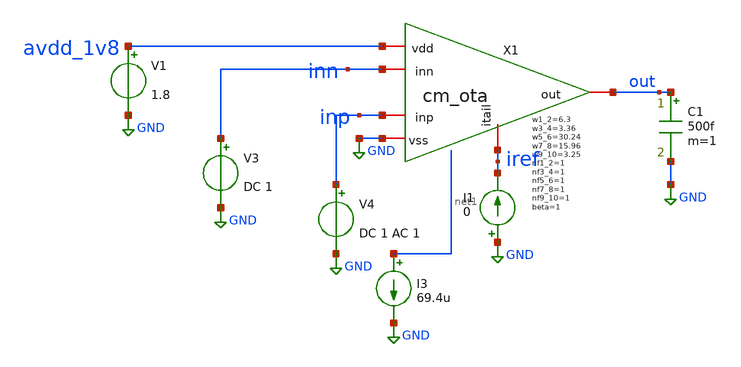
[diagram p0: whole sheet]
** sch_path: ISSCC25/submitted_notebooks/current_mirror_ota_optimization/characterization/sky130/schematics/tb_cm_ota_working_v2_extracted_ac_to_layout.sch
**.subckt tb_cm_ota_working_v2_extracted_ac_to_layout
V1 avdd_1v8 GND 1.8
C1 out GND 500f m=1
V3 inn GND DC 1
V4 inp GND DC 1 AC 1
X1 avdd_1v8 out inp inn iref GND cm_ota w1_2=6.3 w3_4=3.36 w5_6=30.24 w7_8=15.96 w9_10=3.25 beta=1
+ nf1_2=1 nf3_4=1 nf5_6=1 nf7_8=1 nf9_10=1
I1 GND iref 0
I3 net1 GND 69.4u
**** begin user architecture code

** opencircuitdesign pdks isntsall
.lib /opt/pdk/open_pdks/sky130/sky130A/libs.tech/ngspice/sky130.lib.spice tt





.temp 27
.option savecurrents
.save all
.control
	ac dec 100 1 1e15
	plot vdb(out) vs frequency
	plot (180*cph(out)/pi) vs frequency
	let phase_vector = 180*cph(out)/pi
	let gain_vector = vdb(out)
	meas ac unity_gain_freq_val when vdb(out)=0
	meas ac dc_gain_val find vdb(out) at=10Hz
	let dc_gain = dc_gain_val
	meas ac p1_val when phase_vector=-45 cross=1
	meas ac p2_val when phase_vector=-135 cross=1
	meas ac three_db when gain_vector=dc_gain_val -3 cross=1
	let p2 = p2_val
	let p1 = p1_val
	let dc_gain = dc_gain_val
	let unity_gain_freq = unity_gain_freq_val
	op
	write tb_cm_ota_working_v2_extracted_ac.raw
	let gm1 = @m.x1.xm1.msky130_fd_pr__nfet_01v8[gm]
	let gm2 = @m.x1.xm2.msky130_fd_pr__nfet_01v8[gm]
	let gm3 = @m.x1.xm3.msky130_fd_pr__pfet_01v8[gm]
	let gm4 = @m.x1.xm4.msky130_fd_pr__pfet_01v8[gm]
	let gm5 = @m.x1.xm5.msky130_fd_pr__nfet_01v8[gm]
	let gm6 = @m.x1.xm6.msky130_fd_pr__nfet_01v8[gm]
	let gm7 = @m.x1.xm7.msky130_fd_pr__pfet_01v8[gm]
	let gm8 = @m.x1.xm8.msky130_fd_pr__pfet_01v8[gm]

	let id1 = @m.x1.xm1.msky130_fd_pr__nfet_01v8[id]
	let id2 = @m.x1.xm2.msky130_fd_pr__nfet_01v8[id]
	let id3 = @m.x1.xm3.msky130_fd_pr__pfet_01v8[id]
	let id4 = @m.x1.xm4.msky130_fd_pr__pfet_01v8[id]
	let id5 = @m.x1.xm5.msky130_fd_pr__nfet_01v8[id]
	let id6 = @m.x1.xm6.msky130_fd_pr__nfet_01v8[id]
	let id7 = @m.x1.xm7.msky130_fd_pr__pfet_01v8[id]
	let id8 = @m.x1.xm8.msky130_fd_pr__pfet_01v8[id]

	let current_scale = id5/id1

	let kgm1 = gm1/id1
	let kgm2 = gm2/id2
	let kgm3 = gm3/id3
	let kgm4 = gm4/id4
	let kgm5 = gm5/id5
	let kgm6 = gm6/id6
	let kgm7 = gm7/id7
	let kgm8 = gm8/id8

	print kgm1
	print kgm2
	print kgm3
	print kgm4
	print kgm5
	print kgm6
	print kgm7
	print kgm8

	print id1
	print id2
	print id3
	print id4
	print id5
	print id6
	print id7
	print id8

	print current_scale
	print dc_gain_val
	print p1_val
	print p2_val
.endc


**** end user architecture code
**.ends

* expanding   symbol:  cm_ota.sym # of pins=6
** sym_path: ISSCC25/submitted_notebooks/current_mirror_ota_optimization/characterization/sky130/schematics/cm_ota.sym
** sch_path: ISSCC25/submitted_notebooks/current_mirror_ota_optimization/characterization/sky130/schematics/cm_ota.sch
.subckt cm_ota vdd out inp inn itail vss  w1_2=1 w3_4=1 w5_6=1 w7_8=1 w9_10=1 beta=2 nf1_2=2 nf3_4=2
+ nf5_6=2 nf7_8=2 nf9_10=2
*.iopin inn
*.iopin inp
*.iopin out
*.iopin vss
*.iopin vdd
*.iopin itail
XM1 ds1_3 inn source source sky130_fd_pr__nfet_01v8 L=0.15 W=w1_2 nf=nf1_2 ad='int((nf+1)/2) * W/nf * 0.29'
+ as='int((nf+2)/2) * W/nf * 0.29' pd='2*int((nf+1)/2) * (W/nf + 0.29)' ps='2*int((nf+2)/2) * (W/nf + 0.29)'
+ nrd='0.29 / W' nrs='0.29 / W' sa=0 sb=0 sd=0 mult=1 m=1
xM3 ds1_3 ds1_3 vdd vdd sky130_fd_pr__pfet_01v8 L=0.15 W=w3_4 nf=nf3_4 ad='int((nf+1)/2) * W/nf * 0.29'
+ as='int((nf+2)/2) * W/nf * 0.29' pd='2*int((nf+1)/2) * (W/nf + 0.29)' ps='2*int((nf+2)/2) * (W/nf + 0.29)'
+ nrd='0.29 / W' nrs='0.29 / W' sa=0 sb=0 sd=0 mult=1 m=1
XM2 ds2_4 inp source source sky130_fd_pr__nfet_01v8 L=0.15 W=w1_2 nf=nf1_2 ad='int((nf+1)/2) * W/nf * 0.29'
+ as='int((nf+2)/2) * W/nf * 0.29' pd='2*int((nf+1)/2) * (W/nf + 0.29)' ps='2*int((nf+2)/2) * (W/nf + 0.29)'
+ nrd='0.29 / W' nrs='0.29 / W' sa=0 sb=0 sd=0 mult=1 m=1
xM4 ds2_4 ds2_4 vdd vdd sky130_fd_pr__pfet_01v8 L=0.15 W=w3_4 nf=nf3_4 ad='int((nf+1)/2) * W/nf * 0.29'
+ as='int((nf+2)/2) * W/nf * 0.29' pd='2*int((nf+1)/2) * (W/nf + 0.29)' ps='2*int((nf+2)/2) * (W/nf + 0.29)'
+ nrd='0.29 / W' nrs='0.29 / W' sa=0 sb=0 sd=0 mult=1 m=1
xM7 ds5_7 ds1_3 vdd vdd sky130_fd_pr__pfet_01v8 L=0.15 W=w7_8 nf=nf7_8 ad='int((nf+1)/2) * W/nf * 0.29'
+ as='int((nf+2)/2) * W/nf * 0.29' pd='2*int((nf+1)/2) * (W/nf + 0.29)' ps='2*int((nf+2)/2) * (W/nf + 0.29)'
+ nrd='0.29 / W' nrs='0.29 / W' sa=0 sb=0 sd=0 mult=1 m=1
XM5 ds5_7 ds5_7 vss vss sky130_fd_pr__nfet_01v8 L=0.15 W=w5_6 nf=nf5_6 ad='int((nf+1)/2) * W/nf * 0.29'
+ as='int((nf+2)/2) * W/nf * 0.29' pd='2*int((nf+1)/2) * (W/nf + 0.29)' ps='2*int((nf+2)/2) * (W/nf + 0.29)'
+ nrd='0.29 / W' nrs='0.29 / W' sa=0 sb=0 sd=0 mult=1 m=1
XM6 out ds5_7 vss vss sky130_fd_pr__nfet_01v8 L=0.15 W=w5_6 nf=nf5_6 ad='int((nf+1)/2) * W/nf * 0.29'
+ as='int((nf+2)/2) * W/nf * 0.29' pd='2*int((nf+1)/2) * (W/nf + 0.29)' ps='2*int((nf+2)/2) * (W/nf + 0.29)'
+ nrd='0.29 / W' nrs='0.29 / W' sa=0 sb=0 sd=0 mult=1 m=1
xM8 out ds2_4 vdd vdd sky130_fd_pr__pfet_01v8 L=0.15 W=w7_8 nf=nf7_8 ad='int((nf+1)/2) * W/nf * 0.29'
+ as='int((nf+2)/2) * W/nf * 0.29' pd='2*int((nf+1)/2) * (W/nf + 0.29)' ps='2*int((nf+2)/2) * (W/nf + 0.29)'
+ nrd='0.29 / W' nrs='0.29 / W' sa=0 sb=0 sd=0 mult=1 m=1
XM9 source itail vss vss sky130_fd_pr__nfet_01v8 L=0.15 W=w9_10 nf=nf9_10 ad='int((nf+1)/2) * W/nf * 0.29'
+ as='int((nf+2)/2) * W/nf * 0.29' pd='2*int((nf+1)/2) * (W/nf + 0.29)' ps='2*int((nf+2)/2) * (W/nf + 0.29)'
+ nrd='0.29 / W' nrs='0.29 / W' sa=0 sb=0 sd=0 mult=1 m=1
XM10 itail itail vss vss sky130_fd_pr__nfet_01v8 L=0.15 W=w9_10 nf=nf1_2 ad='int((nf+1)/2) * W/nf * 0.29'
+ as='int((nf+2)/2) * W/nf * 0.29' pd='2*int((nf+1)/2) * (W/nf + 0.29)' ps='2*int((nf+2)/2) * (W/nf + 0.29)'
+ nrd='0.29 / W' nrs='0.29 / W' sa=0 sb=0 sd=0 mult=1 m=1
.ends

.GLOBAL GND
.end
